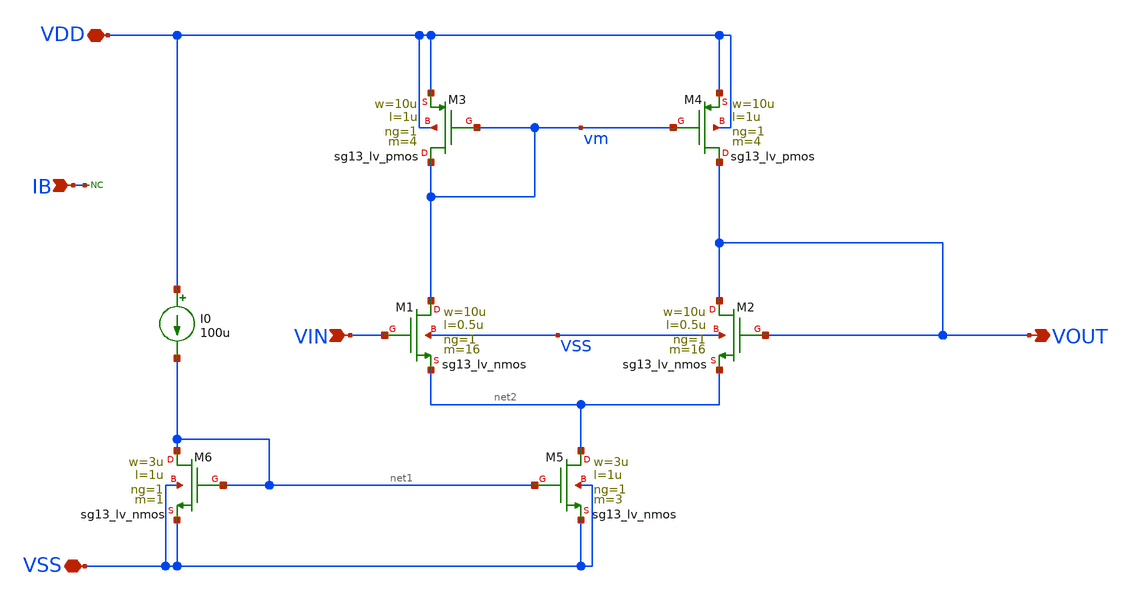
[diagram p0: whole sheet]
** sch_path: OTA_Telescopic_NO_FLATTEN/Schematics_and_Symbols/Buffer2.sch
**.subckt Buffer2 VDD VSS VIN VOUT IB
*.iopin VDD
*.iopin VSS
*.ipin VIN
*.opin VOUT
*.ipin IB
XM5 net2 net1 VSS VSS sg13_lv_nmos w=3u l=1u ng=1 m=3 mm_ok=1
XM6 net1 net1 VSS VSS sg13_lv_nmos w=3u l=1u ng=1 m=1 mm_ok=1
XM1 vm VIN net2 VSS sg13_lv_nmos w=10u l=0.5u ng=1 m=16 mm_ok=1
XM2 VOUT VOUT net2 VSS sg13_lv_nmos w=10u l=0.5u ng=1 m=16 mm_ok=1
XM3 vm vm VDD VDD sg13_lv_pmos w=10u l=1u ng=1 m=4 mm_ok=1
XM4 VOUT vm VDD VDD sg13_lv_pmos w=10u l=1u ng=1 m=4 mm_ok=1
I0 VDD net1 100u
* noconn IB
**.ends
.end
